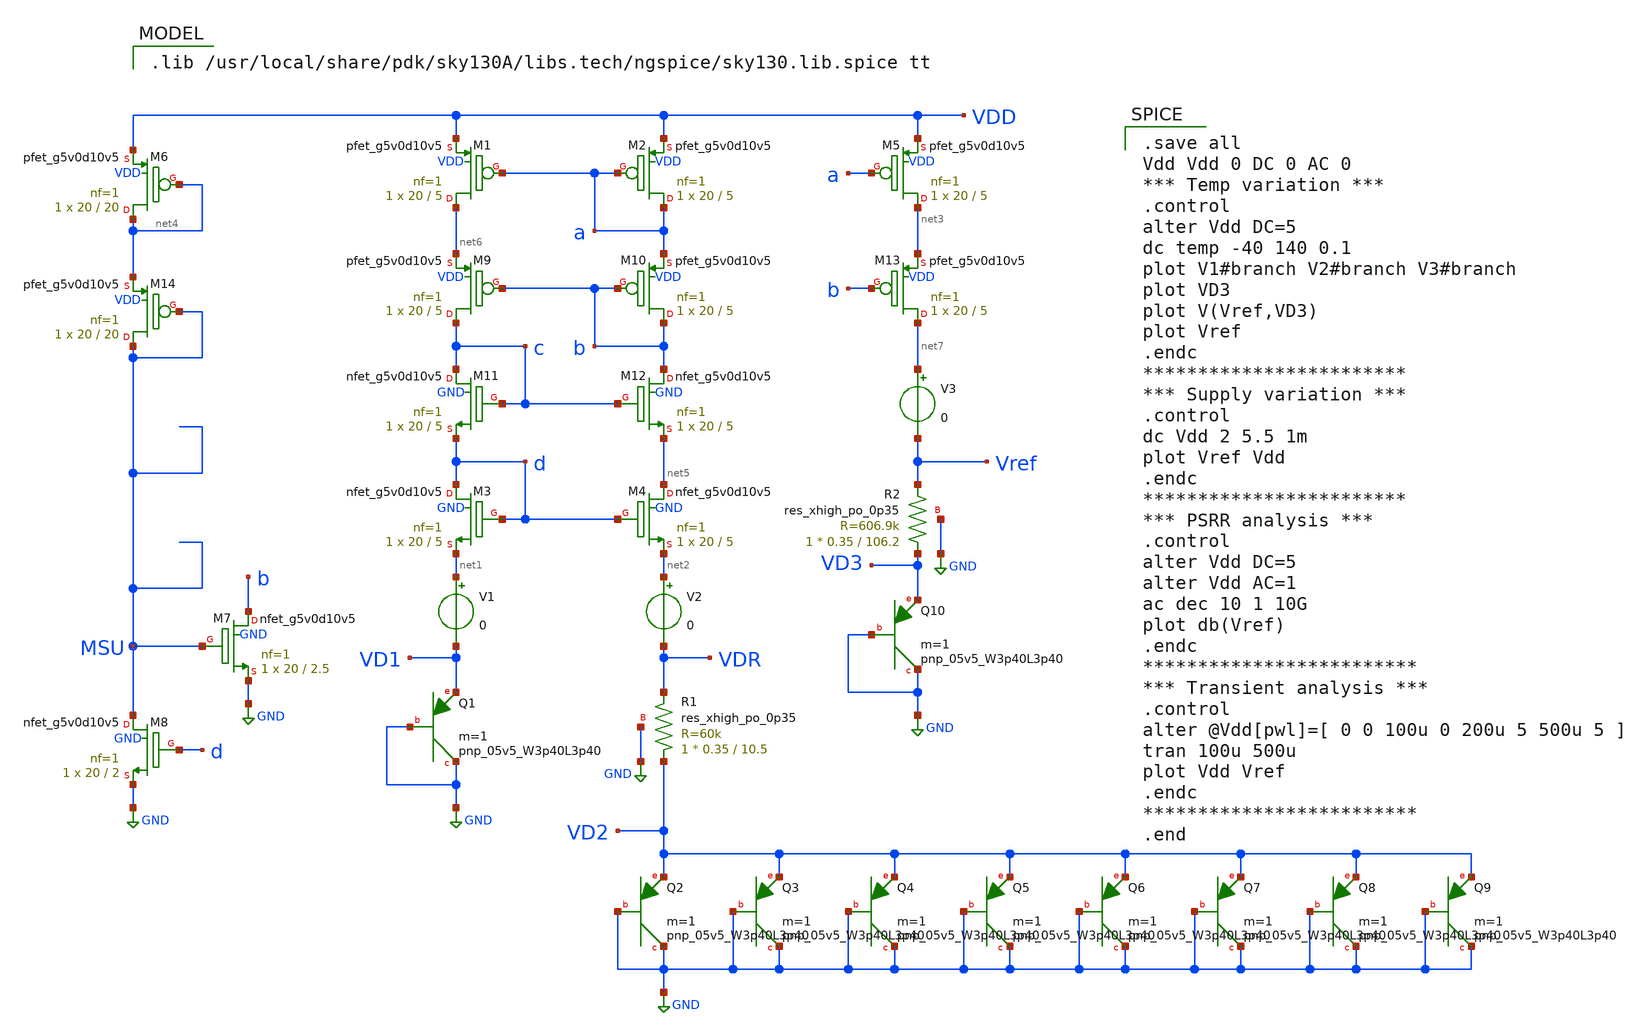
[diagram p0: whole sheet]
** sch_path: 3_BGR_cas_60k_3p4pnp.sch
**.subckt 3_BGR_cas_60k_3p4pnp
V1 net1 VD1 0
V2 net2 VDR 0
V3 net7 Vref 0
XR1 VD2 VDR GND sky130_fd_pr__res_xhigh_po_0p35 L=10.5 mult=1 m=1
XR2 VD3 Vref GND sky130_fd_pr__res_xhigh_po_0p35 L=106.2 mult=1 m=1
XM1 net6 a VDD VDD sky130_fd_pr__pfet_g5v0d10v5 L=5 W=20 nf=1 ad='int((nf+1)/2) * W/nf * 0.29' as='int((nf+2)/2) * W/nf * 0.29'
+ pd='2*int((nf+1)/2) * (W/nf + 0.29)' ps='2*int((nf+2)/2) * (W/nf + 0.29)' nrd='0.29 / W' nrs='0.29 / W'
+ sa=0 sb=0 sd=0 mult=1 m=1
XM2 a a VDD VDD sky130_fd_pr__pfet_g5v0d10v5 L=5 W=20 nf=1 ad='int((nf+1)/2) * W/nf * 0.29' as='int((nf+2)/2) * W/nf * 0.29'
+ pd='2*int((nf+1)/2) * (W/nf + 0.29)' ps='2*int((nf+2)/2) * (W/nf + 0.29)' nrd='0.29 / W' nrs='0.29 / W'
+ sa=0 sb=0 sd=0 mult=1 m=1
XM3 d d net1 GND sky130_fd_pr__nfet_g5v0d10v5 L=5 W=20 nf=1 ad='int((nf+1)/2) * W/nf * 0.29' as='int((nf+2)/2) * W/nf * 0.29'
+ pd='2*int((nf+1)/2) * (W/nf + 0.29)' ps='2*int((nf+2)/2) * (W/nf + 0.29)' nrd='0.29 / W' nrs='0.29 / W'
+ sa=0 sb=0 sd=0 mult=1 m=1
XM4 net5 d net2 GND sky130_fd_pr__nfet_g5v0d10v5 L=5 W=20 nf=1 ad='int((nf+1)/2) * W/nf * 0.29' as='int((nf+2)/2) * W/nf * 0.29'
+ pd='2*int((nf+1)/2) * (W/nf + 0.29)' ps='2*int((nf+2)/2) * (W/nf + 0.29)' nrd='0.29 / W' nrs='0.29 / W'
+ sa=0 sb=0 sd=0 mult=1 m=1
XM5 net3 a VDD VDD sky130_fd_pr__pfet_g5v0d10v5 L=5 W=20 nf=1 ad='int((nf+1)/2) * W/nf * 0.29' as='int((nf+2)/2) * W/nf * 0.29'
+ pd='2*int((nf+1)/2) * (W/nf + 0.29)' ps='2*int((nf+2)/2) * (W/nf + 0.29)' nrd='0.29 / W' nrs='0.29 / W'
+ sa=0 sb=0 sd=0 mult=1 m=1
XM8 MSU d GND GND sky130_fd_pr__nfet_g5v0d10v5 L=2 W=20 nf=1 ad='int((nf+1)/2) * W/nf * 0.29' as='int((nf+2)/2) * W/nf * 0.29'
+ pd='2*int((nf+1)/2) * (W/nf + 0.29)' ps='2*int((nf+2)/2) * (W/nf + 0.29)' nrd='0.29 / W' nrs='0.29 / W'
+ sa=0 sb=0 sd=0 mult=1 m=1
XM7 b MSU GND GND sky130_fd_pr__nfet_g5v0d10v5 L=2.5 W=20 nf=1 ad='int((nf+1)/2) * W/nf * 0.29' as='int((nf+2)/2) * W/nf * 0.29'
+ pd='2*int((nf+1)/2) * (W/nf + 0.29)' ps='2*int((nf+2)/2) * (W/nf + 0.29)' nrd='0.29 / W' nrs='0.29 / W'
+ sa=0 sb=0 sd=0 mult=1 m=1
XQ1 GND GND VD1 sky130_fd_pr__pnp_05v5_W3p40L3p40 m=1
XQ2 GND GND VD2 sky130_fd_pr__pnp_05v5_W3p40L3p40 m=1
XQ3 GND GND VD2 sky130_fd_pr__pnp_05v5_W3p40L3p40 m=1
XQ4 GND GND VD2 sky130_fd_pr__pnp_05v5_W3p40L3p40 m=1
XQ5 GND GND VD2 sky130_fd_pr__pnp_05v5_W3p40L3p40 m=1
XQ6 GND GND VD2 sky130_fd_pr__pnp_05v5_W3p40L3p40 m=1
XQ7 GND GND VD2 sky130_fd_pr__pnp_05v5_W3p40L3p40 m=1
XQ8 GND GND VD2 sky130_fd_pr__pnp_05v5_W3p40L3p40 m=1
XQ9 GND GND VD2 sky130_fd_pr__pnp_05v5_W3p40L3p40 m=1
XQ10 GND GND VD3 sky130_fd_pr__pnp_05v5_W3p40L3p40 m=1
XM6 net4 net4 VDD VDD sky130_fd_pr__pfet_g5v0d10v5 L=20 W=20 nf=1 ad='int((nf+1)/2) * W/nf * 0.29' as='int((nf+2)/2) * W/nf * 0.29'
+ pd='2*int((nf+1)/2) * (W/nf + 0.29)' ps='2*int((nf+2)/2) * (W/nf + 0.29)' nrd='0.29 / W' nrs='0.29 / W'
+ sa=0 sb=0 sd=0 mult=1 m=1
XM9 c b net6 VDD sky130_fd_pr__pfet_g5v0d10v5 L=5 W=20 nf=1 ad='int((nf+1)/2) * W/nf * 0.29' as='int((nf+2)/2) * W/nf * 0.29'
+ pd='2*int((nf+1)/2) * (W/nf + 0.29)' ps='2*int((nf+2)/2) * (W/nf + 0.29)' nrd='0.29 / W' nrs='0.29 / W'
+ sa=0 sb=0 sd=0 mult=1 m=1
XM10 b b a VDD sky130_fd_pr__pfet_g5v0d10v5 L=5 W=20 nf=1 ad='int((nf+1)/2) * W/nf * 0.29' as='int((nf+2)/2) * W/nf * 0.29'
+ pd='2*int((nf+1)/2) * (W/nf + 0.29)' ps='2*int((nf+2)/2) * (W/nf + 0.29)' nrd='0.29 / W' nrs='0.29 / W'
+ sa=0 sb=0 sd=0 mult=1 m=1
XM11 c c d GND sky130_fd_pr__nfet_g5v0d10v5 L=5 W=20 nf=1 ad='int((nf+1)/2) * W/nf * 0.29' as='int((nf+2)/2) * W/nf * 0.29'
+ pd='2*int((nf+1)/2) * (W/nf + 0.29)' ps='2*int((nf+2)/2) * (W/nf + 0.29)' nrd='0.29 / W' nrs='0.29 / W'
+ sa=0 sb=0 sd=0 mult=1 m=1
XM12 b c net5 GND sky130_fd_pr__nfet_g5v0d10v5 L=5 W=20 nf=1 ad='int((nf+1)/2) * W/nf * 0.29' as='int((nf+2)/2) * W/nf * 0.29'
+ pd='2*int((nf+1)/2) * (W/nf + 0.29)' ps='2*int((nf+2)/2) * (W/nf + 0.29)' nrd='0.29 / W' nrs='0.29 / W'
+ sa=0 sb=0 sd=0 mult=1 m=1
XM13 net7 b net3 VDD sky130_fd_pr__pfet_g5v0d10v5 L=5 W=20 nf=1 ad='int((nf+1)/2) * W/nf * 0.29' as='int((nf+2)/2) * W/nf * 0.29'
+ pd='2*int((nf+1)/2) * (W/nf + 0.29)' ps='2*int((nf+2)/2) * (W/nf + 0.29)' nrd='0.29 / W' nrs='0.29 / W'
+ sa=0 sb=0 sd=0 mult=1 m=1
XM14 MSU MSU net4 VDD sky130_fd_pr__pfet_g5v0d10v5 L=20 W=20 nf=1 ad='int((nf+1)/2) * W/nf * 0.29' as='int((nf+2)/2) * W/nf * 0.29'
+ pd='2*int((nf+1)/2) * (W/nf + 0.29)' ps='2*int((nf+2)/2) * (W/nf + 0.29)' nrd='0.29 / W' nrs='0.29 / W'
+ sa=0 sb=0 sd=0 mult=1 m=1
**** begin user architecture code

.lib /usr/local/share/pdk/sky130A/libs.tech/ngspice/sky130.lib.spice tt


.save all
Vdd Vdd 0 DC 0 AC 0
*** Temp variation ***
.control
alter Vdd DC=5
dc temp -40 140 0.1
plot V1#branch V2#branch V3#branch
plot VD3
plot V(Vref,VD3)
plot Vref
.endc
************************
*** Supply variation ***
.control
dc Vdd 2 5.5 1m
plot Vref Vdd
.endc
************************
*** PSRR analysis ***
.control
alter Vdd DC=5
alter Vdd AC=1
ac dec 10 1 10G
plot db(Vref)
.endc
*************************
*** Transient analysis ***
.control
alter @Vdd[pwl]=[ 0 0 100u 0 200u 5 500u 5 ]
tran 100u 500u
plot Vdd Vref
.endc
*************************
.end

**** end user architecture code
**.ends
.GLOBAL GND
.end
